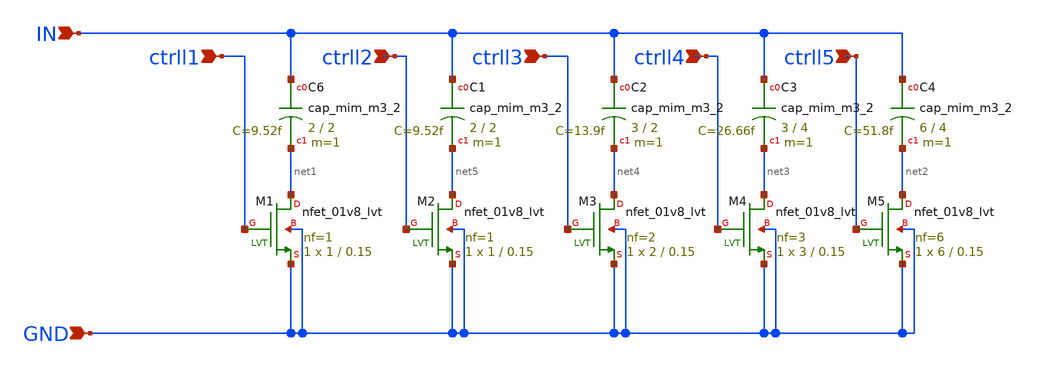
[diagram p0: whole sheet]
** sch_path: design/vco/1.7G~10G/schematic/cap_bank.sch
**.subckt cap_bank IN GND ctrll1 ctrll2 ctrll3 ctrll4 ctrll5
*.ipin IN
*.ipin GND
*.ipin ctrll1
*.ipin ctrll2
*.ipin ctrll3
*.ipin ctrll4
*.ipin ctrll5
XC6 IN net1 sky130_fd_pr__cap_mim_m3_2 W=2 L=2 MF=1 m=1
XC1 IN net5 sky130_fd_pr__cap_mim_m3_2 W=2 L=2 MF=1 m=1
XC2 IN net4 sky130_fd_pr__cap_mim_m3_2 W=3 L=2 MF=1 m=1
XC3 IN net3 sky130_fd_pr__cap_mim_m3_2 W=3 L=4 MF=1 m=1
XC4 IN net2 sky130_fd_pr__cap_mim_m3_2 W=6 L=4 MF=1 m=1
XM1 net1 ctrll1 GND GND sky130_fd_pr__nfet_01v8_lvt L=0.15 W=1 nf=1 ad='int((nf+1)/2) * W/nf * 0.29'
+ as='int((nf+2)/2) * W/nf * 0.29' pd='2*int((nf+1)/2) * (W/nf + 0.29)' ps='2*int((nf+2)/2) * (W/nf + 0.29)'
+ nrd='0.29 / W' nrs='0.29 / W' sa=0 sb=0 sd=0 mult=1 m=1
XM2 net5 ctrll2 GND GND sky130_fd_pr__nfet_01v8_lvt L=0.15 W=1 nf=1 ad='int((nf+1)/2) * W/nf * 0.29'
+ as='int((nf+2)/2) * W/nf * 0.29' pd='2*int((nf+1)/2) * (W/nf + 0.29)' ps='2*int((nf+2)/2) * (W/nf + 0.29)'
+ nrd='0.29 / W' nrs='0.29 / W' sa=0 sb=0 sd=0 mult=1 m=1
XM3 net4 ctrll3 GND GND sky130_fd_pr__nfet_01v8_lvt L=0.15 W=2 nf=2 ad='int((nf+1)/2) * W/nf * 0.29'
+ as='int((nf+2)/2) * W/nf * 0.29' pd='2*int((nf+1)/2) * (W/nf + 0.29)' ps='2*int((nf+2)/2) * (W/nf + 0.29)'
+ nrd='0.29 / W' nrs='0.29 / W' sa=0 sb=0 sd=0 mult=1 m=1
XM4 net3 ctrll4 GND GND sky130_fd_pr__nfet_01v8_lvt L=0.15 W=3 nf=3 ad='int((nf+1)/2) * W/nf * 0.29'
+ as='int((nf+2)/2) * W/nf * 0.29' pd='2*int((nf+1)/2) * (W/nf + 0.29)' ps='2*int((nf+2)/2) * (W/nf + 0.29)'
+ nrd='0.29 / W' nrs='0.29 / W' sa=0 sb=0 sd=0 mult=1 m=1
XM5 net2 ctrll5 GND GND sky130_fd_pr__nfet_01v8_lvt L=0.15 W=6 nf=6 ad='int((nf+1)/2) * W/nf * 0.29'
+ as='int((nf+2)/2) * W/nf * 0.29' pd='2*int((nf+1)/2) * (W/nf + 0.29)' ps='2*int((nf+2)/2) * (W/nf + 0.29)'
+ nrd='0.29 / W' nrs='0.29 / W' sa=0 sb=0 sd=0 mult=1 m=1
**.ends
.end
